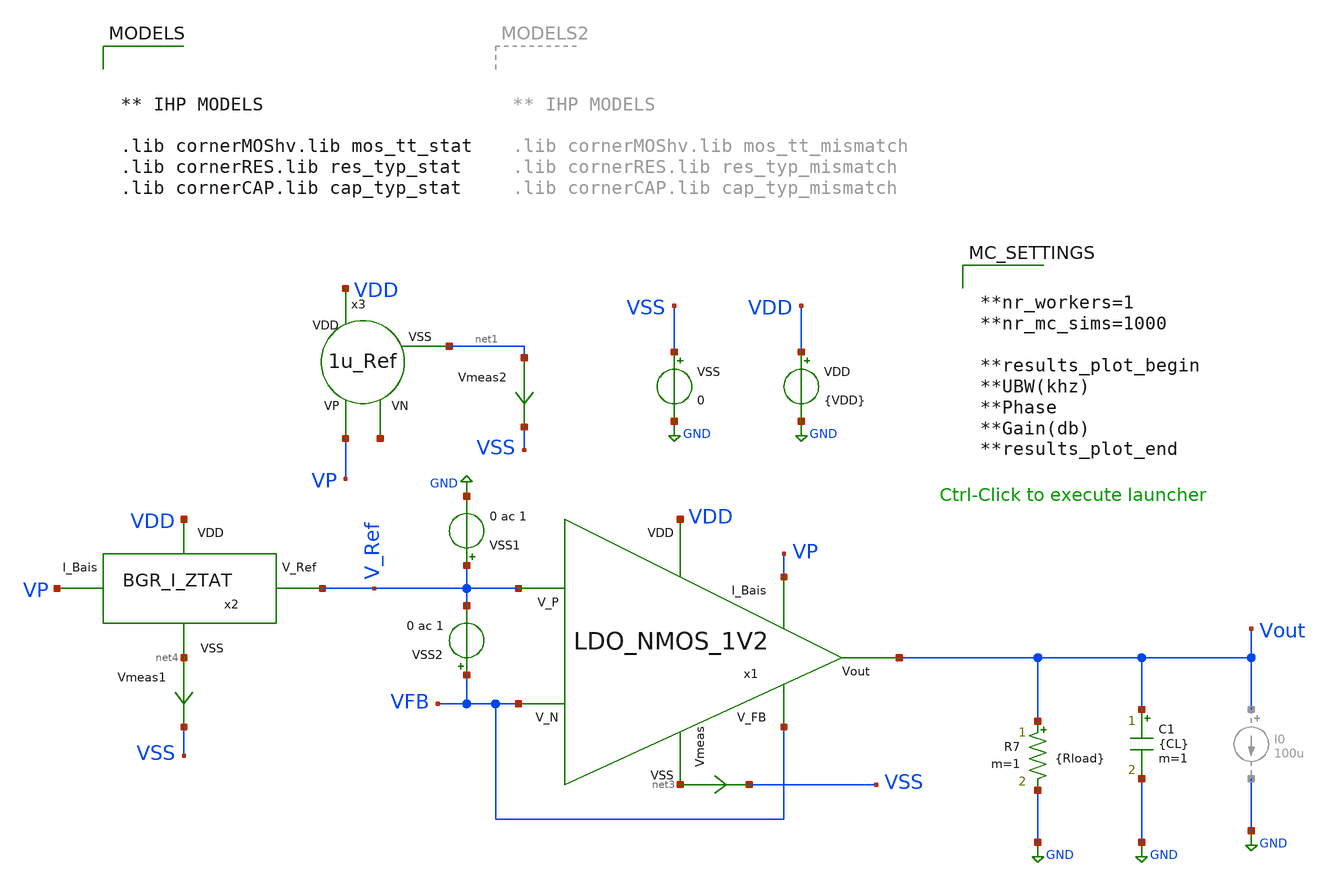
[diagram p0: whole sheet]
** sch_path: dependencies/PMU/PMU-main/testbenches/mc/xschem/PMU_AC_Stability_TB_MC.sch
**.subckt PMU_AC_Stability_TB_MC
VDD VDD GND {VDD}
Vmeas2 net1 VSS 0
.save i(vmeas2)
VSS VSS GND 0
C1 Vout GND {CL} m=1
R7 Vout GND {Rload} m=1
x3 VDD VP net2 net1 1u_Ref
x1 VDD VP V_Ref VFB Vout VFB net3 LDO_NMOS_1V2
Vmeas net3 VSS 0
.save i(vmeas)
Vmeas1 net4 VSS 0
.save i(vmeas1)
x2 VDD net4 V_Ref VP BGR_I_ZTAT
VSS1 V_Ref GND 0 ac 1
VSS2 VFB V_Ref 0 ac 1
**** begin user architecture code



** IHP MODELS

.lib cornerMOShv.lib mos_tt_stat
.lib cornerRES.lib res_typ_stat
.lib cornerCAP.lib cap_typ_stat





.include LDO_DC_TB.save
.save all
.options rshunt = 1e12
.options gmin=1e-12
.options reltol = 0.01 abstol = 1p
.param temp = 27
.param CL = 100p
.param Rload = 12k
.param VDD = 3
.control

save all

	ac dec 100 1 100g
	let G_P = db(Vout)
	let PH_P = 180*cph(Vout)/Pi
	meas ac UBW when G_P = 0
	meas ac Phase FIND PH_P at=UBW
	meas ac Gain(db) FIND G_P at=1
let UBW(khz) = UBW/1000
echo results_save_begin
print UBW(khz)
print Phase
print Gain(db)
echo results_save_end
.endc




**nr_workers=1
**nr_mc_sims=1000

**results_plot_begin
**UBW(khz)
**Phase
**Gain(db)
**results_plot_end


**** end user architecture code
**.ends

* expanding   symbol:  1u_Ref.sym # of pins=4
** sym_path: dependencies/PMU/PMU-main/schematic/xschem/1u_Ref.sym
** sch_path: dependencies/PMU/PMU-main/schematic/xschem/1u_Ref.sch
.subckt 1u_Ref VDD VP VN VSS
*.iopin VDD
*.iopin VSS
*.iopin VP
*.iopin VN
XM1 VP VP VDD VDD sg13_hv_pmos w=10u l=2u ng=1 m=1 mm_ok=1
XM2 VN VP VDD VDD sg13_hv_pmos w=10u l=2u ng=1 m=1 mm_ok=1
XM6 net1 net1 VDD VDD sg13_hv_pmos w=0.3u l=10u ng=1 m=1 mm_ok=1
XM7 V1 VN net4 net4 sg13_hv_nmos w=1u l=6u ng=1 m=1 mm_ok=1
XM5 net3 V1 VN VSS sg13_hv_nmos w=1u l=10u ng=1 m=1 mm_ok=1
Vmeas2 net2 VSS 0
.save i(vmeas2)
XM4 VN VR net2 net2 sg13_hv_nmos w=10u l=1u ng=1 m=1 mm_ok=1
XM3 net5 VN VR VSS sg13_hv_nmos w=10u l=1u ng=1 m=4 mm_ok=1
Vmeas1 VP net5 0
.save i(vmeas1)
Vmeas3 VP net3 0
.save i(vmeas3)
Vmeas4 net4 VSS 0
.save i(vmeas4)
XM8 V1 V1 net1 VDD sg13_hv_pmos w=0.3u l=10u ng=1 m=1 mm_ok=1
XR1 VR VSS sub! rhigh w=0.5e-6 l=185e-6 m=1 b=0 mm_ok=1
.ends


* expanding   symbol:  LDO_NMOS_1V2.sym # of pins=7
** sym_path: dependencies/PMU/PMU-main/schematic/xschem/LDO_NMOS_1V2.sym
** sch_path: dependencies/PMU/PMU-main/schematic/xschem/LDO_NMOS_1V2.sch
.subckt LDO_NMOS_1V2 VDD I_Bais V_P V_N Vout V_FB VSS
*.iopin Vout
*.iopin VDD
*.iopin I_Bais
*.iopin V_P
*.iopin V_N
*.iopin V_FB
*.iopin VSS
Vmeas net6 VSS 0
.save i(vmeas)
XM6 VDD VG2 Vout GND sg13_hv_nmos w=10u l=0.45u ng=10 m=50 mm_ok=1
XR3 Vout V_FB sub! rhigh w=0.5e-6 l=18e-6 m=2 b=0 mm_ok=1
Vmeas1 net5 VSS 0
.save i(vmeas1)
XR2 V_FB net3 sub! rhigh w=0.5e-6 l=18e-6 m=2 b=0 mm_ok=1
XR4 net3 net2 sub! rhigh w=0.5e-6 l=18e-6 m=2 b=0 mm_ok=1
XR5 net2 net5 sub! rhigh w=0.5e-6 l=18e-6 m=2 b=0 mm_ok=1
x1 VDD I_Bais V_N V_P net1 VG2 net6 OpAmp_2etags
XC3 net4 net1 cap_cmim w=33.24e-6 l=50.0e-6 m=3 mm_ok=1
XC4 VG2 net5 cap_cmim w=33.24e-6 l=50e-6 m=2 mm_ok=1
XR1 VG2 net4 sub! rhigh w=0.5e-6 l=15e-6 m=1 b=0 mm_ok=1
.ends


* expanding   symbol:  /foss/designs/bgr/BGR_I_ZTAT.sym # of pins=4
** sym_path: dependencies/PMU/PMU-main/schematic/xschem/BGR_I_ZTAT.sym
** sch_path: dependencies/PMU/PMU-main/schematic/xschem/BGR_I_ZTAT.sch
.subckt BGR_I_ZTAT VDD VSS V_Ref I_Bais
*.iopin VDD
*.iopin I_Bais
*.iopin V_Ref
*.iopin VSS
XM7 net2 V_out VDD VDD sg13_hv_pmos w=1u l=3u ng=1 m=1 mm_ok=1
XM8 net3 V_out VDD VDD sg13_hv_pmos w=1u l=3u ng=1 m=1 mm_ok=1
XC1 VDD V_out cap_cmim w=13.265e-6 l=50e-6 m=1 mm_ok=1
Vmeas1 net3 Vp 0
.save i(vmeas1)
Vmeas22 Vn net1 0
.save i(vmeas22)
x2 VDD I_Bais Vp Vn V_out net5 Stage1
XM2 Vp1 Vp1 VSS VSS sg13_hv_nmos w=7.5u l=4u ng=1 m=2 mm_ok=1
XM3 net1 net1 VSS VSS sg13_hv_nmos w=7.5u l=4u ng=1 m=1 mm_ok=1
Vmeas2 net2 Vn 0
.save i(vmeas2)
Vmeas5 net4 Vp1 0
.save i(vmeas5)
Vmeas6 net5 VSS 0
.save i(vmeas6)
XM1 V_Ref V_out VDD VDD sg13_hv_pmos w=1u l=3u ng=1 m=1 mm_ok=1
Vmeas3 V_Ref net11 0
.save i(vmeas3)
XM4 net11 net11 VSS VSS sg13_hv_nmos w=2u l=2.75u ng=1 m=1 mm_ok=1
XM6 net8 Vn VSS GND sg13_hv_nmos w=4u l=2u ng=1 m=1 mm_ok=1
XM5 net6 net6 VDD VDD sg13_hv_pmos w=4u l=1u ng=1 m=1 mm_ok=1
XM9 net7 net6 VDD VDD sg13_hv_pmos w=4u l=1u ng=1 m=1 mm_ok=1
Vmeas4 net7 net8 0
.save i(vmeas4)
XC3 net9 VSS cap_cmim w=5e-6 l=5e-6 m=1 mm_ok=1
XM10 VSS VDD net6 VDD sg13_hv_pmos w=4u l=1u ng=1 m=1 mm_ok=1
XMSU V_out net8 net10 net10 sg13_hv_nmos w=4u l=2u ng=1 m=1 mm_ok=1
Vmeas8 net6 net9 0
.save i(vmeas8)
Vmeas9 net10 VSS 0
.save i(vmeas9)
XR4 Vp VSS sub! rhigh w=0.5e-6 l=80e-6 m=1 b=0 mm_ok=1
XR5 Vp net4 sub! rhigh w=0.5e-6 l=210e-6 m=1 b=0 mm_ok=1
.ends


* expanding   symbol:  OpAmp_2etags.sym # of pins=7
** sym_path: dependencies/PMU/PMU-main/schematic/xschem/OpAmp_2etags.sym
** sch_path: dependencies/PMU/PMU-main/schematic/xschem/OpAmp_2etags.sch
.subckt OpAmp_2etags VDD I_Bais VP VN VG VOUT VSS
*.iopin VDD
*.iopin I_Bais
*.iopin VP
*.iopin VN
*.iopin VG
*.iopin VOUT
*.iopin VSS
XM3 VX2 VX2 VSS VSS sg13_hv_nmos w=10u l=2u ng=1 m=2 mm_ok=1
XM1 VX2 VP net1 VDD sg13_hv_pmos w=5u l=2u ng=1 m=2 mm_ok=1
XM2 VG VN net1 VDD sg13_hv_pmos w=5u l=2u ng=1 m=2 mm_ok=1
XM4 VG VX2 VSS VSS sg13_hv_nmos w=10u l=2u ng=1 m=2 mm_ok=1
XM5 net1 I_Bais VDD VDD sg13_hv_pmos w=10u l=2u ng=1 m=4 mm_ok=1
XM7 VOUT I_Bais VDD VDD sg13_hv_pmos w=10u l=2u ng=1 m=8 mm_ok=1
XM6 VOUT VG VSS VSS sg13_hv_nmos w=10u l=2u ng=1 m=8 mm_ok=1
.ends


* expanding   symbol:  Stage1.sym # of pins=6
** sym_path: dependencies/PMU/PMU-main/schematic/xschem/Stage1.sym
** sch_path: dependencies/PMU/PMU-main/schematic/xschem/Stage1.sch
.subckt Stage1 VDD VB Vin1 Vin2 Vout1 VSS
*.iopin VDD
*.ipin VB
*.ipin Vin1
*.ipin Vin2
*.iopin VSS
*.opin Vout1
XM1 net1 Vin1 VX VDD sg13_hv_pmos w=10u l=5u ng=2 m=2 mm_ok=1
XM2 net1 net1 VSS VSS sg13_hv_nmos w=1u l=10u ng=2 m=2 mm_ok=1
XM3 Vout1 net1 VSS VSS sg13_hv_nmos w=1u l=10u ng=2 m=2 mm_ok=1
XM4 Vout1 Vin2 VX VDD sg13_hv_pmos w=10u l=5u ng=2 m=2 mm_ok=1
XM5 VX VB VDD VDD sg13_hv_pmos w=10u l=2u ng=1 m=5 mm_ok=1
.ends

.GLOBAL GND
.end
